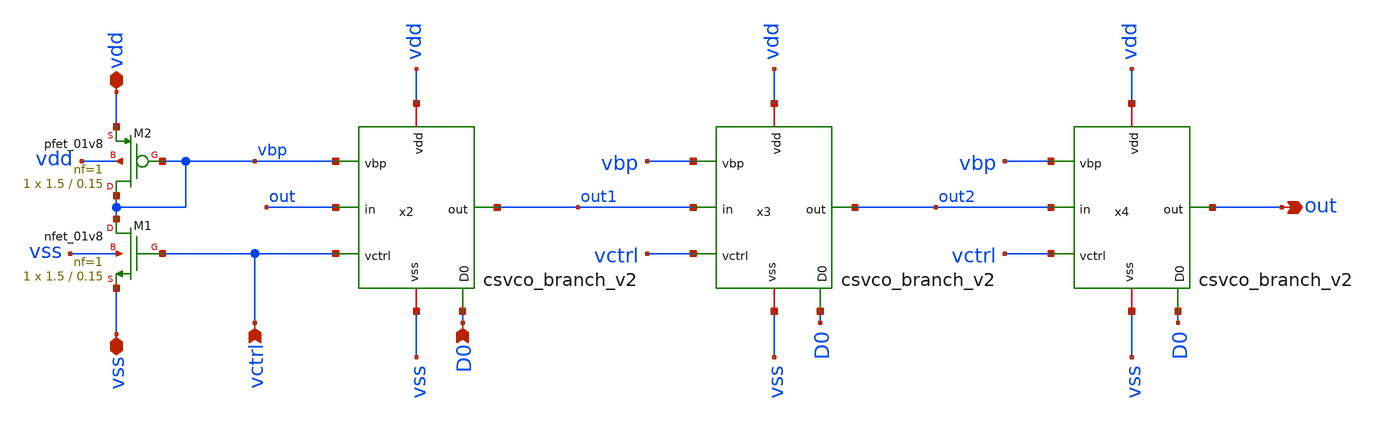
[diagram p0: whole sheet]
** sch_path: xschem/csvco_v2.sch
**.subckt csvco_v2 vctrl vss vdd out D0
*.ipin vctrl
*.iopin vss
*.iopin vdd
*.opin out
*.ipin D0
XM1 vbp vctrl vss vss sky130_fd_pr__nfet_01v8 L=0.15 W=1.5 nf=1 ad='int((nf+1)/2) * W/nf * 0.29' as='int((nf+2)/2) * W/nf * 0.29'
+ pd='2*int((nf+1)/2) * (W/nf + 0.29)' ps='2*int((nf+2)/2) * (W/nf + 0.29)' nrd='0.29 / W' nrs='0.29 / W'
+ sa=0 sb=0 sd=0 mult=1 m=1
XM2 vbp vbp vdd vdd sky130_fd_pr__pfet_01v8 L=0.15 W=1.5 nf=1 ad='int((nf+1)/2) * W/nf * 0.29' as='int((nf+2)/2) * W/nf * 0.29'
+ pd='2*int((nf+1)/2) * (W/nf + 0.29)' ps='2*int((nf+2)/2) * (W/nf + 0.29)' nrd='0.29 / W' nrs='0.29 / W'
+ sa=0 sb=0 sd=0 mult=1 m=1
x2 vdd vbp out out1 vctrl vss D0 csvco_branch_v2
x3 vdd vbp out1 out2 vctrl vss D0 csvco_branch_v2
x4 vdd vbp out2 out vctrl vss D0 csvco_branch_v2
**.ends

* expanding   symbol:  csvco_branch_v2.sym # of pins=7
** sym_path: xschem/csvco_branch_v2.sym
** sch_path: xschem/csvco_branch_v2.sch
.subckt csvco_branch_v2 vdd vbp in out vctrl vss D0
*.ipin vctrl
*.ipin vbp
*.iopin vdd
*.iopin vss
*.ipin in
*.opin out
*.ipin D0
XM1 vdd_inv vbp vdd vdd sky130_fd_pr__pfet_01v8 L=0.15 W=1.5 nf=1 ad='int((nf+1)/2) * W/nf * 0.29' as='int((nf+2)/2) * W/nf * 0.29'
+ pd='2*int((nf+1)/2) * (W/nf + 0.29)' ps='2*int((nf+2)/2) * (W/nf + 0.29)' nrd='0.29 / W' nrs='0.29 / W'
+ sa=0 sb=0 sd=0 mult=1 m=1
XM2 vss_inv vctrl vss vss sky130_fd_pr__nfet_01v8 L=0.15 W=1.5 nf=1 ad='int((nf+1)/2) * W/nf * 0.29'
+ as='int((nf+2)/2) * W/nf * 0.29' pd='2*int((nf+1)/2) * (W/nf + 0.29)' ps='2*int((nf+2)/2) * (W/nf + 0.29)'
+ nrd='0.29 / W' nrs='0.29 / W' sa=0 sb=0 sd=0 mult=1 m=1
XM4 out D0 net1 vss sky130_fd_pr__nfet_01v8 L=0.15 W=0.42 nf=1 ad='int((nf+1)/2) * W/nf * 0.29' as='int((nf+2)/2) * W/nf * 0.29'
+ pd='2*int((nf+1)/2) * (W/nf + 0.29)' ps='2*int((nf+2)/2) * (W/nf + 0.29)' nrd='0.29 / W' nrs='0.29 / W'
+ sa=0 sb=0 sd=0 mult=1 m=1
C1 net1 vss 5.78f m=1
x1 vdd_inv out in vss_inv vdd vss inverter_csvco
.ends


* expanding   symbol:  inverter_csvco.sym # of pins=6
** sym_path: xschem/inverter_csvco.sym
** sch_path: xschem/inverter_csvco.sch
.subckt inverter_csvco vdd out in vss vbulkp vbulkn
*.iopin vss
*.ipin in
*.opin out
*.iopin vdd
*.iopin vbulkn
*.iopin vbulkp
XM1 out in vss vbulkn sky130_fd_pr__nfet_01v8 L=0.2 W=0.75 nf=1 ad='int((nf+1)/2) * W/nf * 0.29' as='int((nf+2)/2) * W/nf * 0.29'
+ pd='2*int((nf+1)/2) * (W/nf + 0.29)' ps='2*int((nf+2)/2) * (W/nf + 0.29)' nrd='0.29 / W' nrs='0.29 / W'
+ sa=0 sb=0 sd=0 mult=1 m=1
XM2 out in vdd vbulkp sky130_fd_pr__pfet_01v8 L=0.2 W=1.5 nf=1 ad='int((nf+1)/2) * W/nf * 0.29' as='int((nf+2)/2) * W/nf * 0.29'
+ pd='2*int((nf+1)/2) * (W/nf + 0.29)' ps='2*int((nf+2)/2) * (W/nf + 0.29)' nrd='0.29 / W' nrs='0.29 / W'
+ sa=0 sb=0 sd=0 mult=1 m=1
.ends

.end
